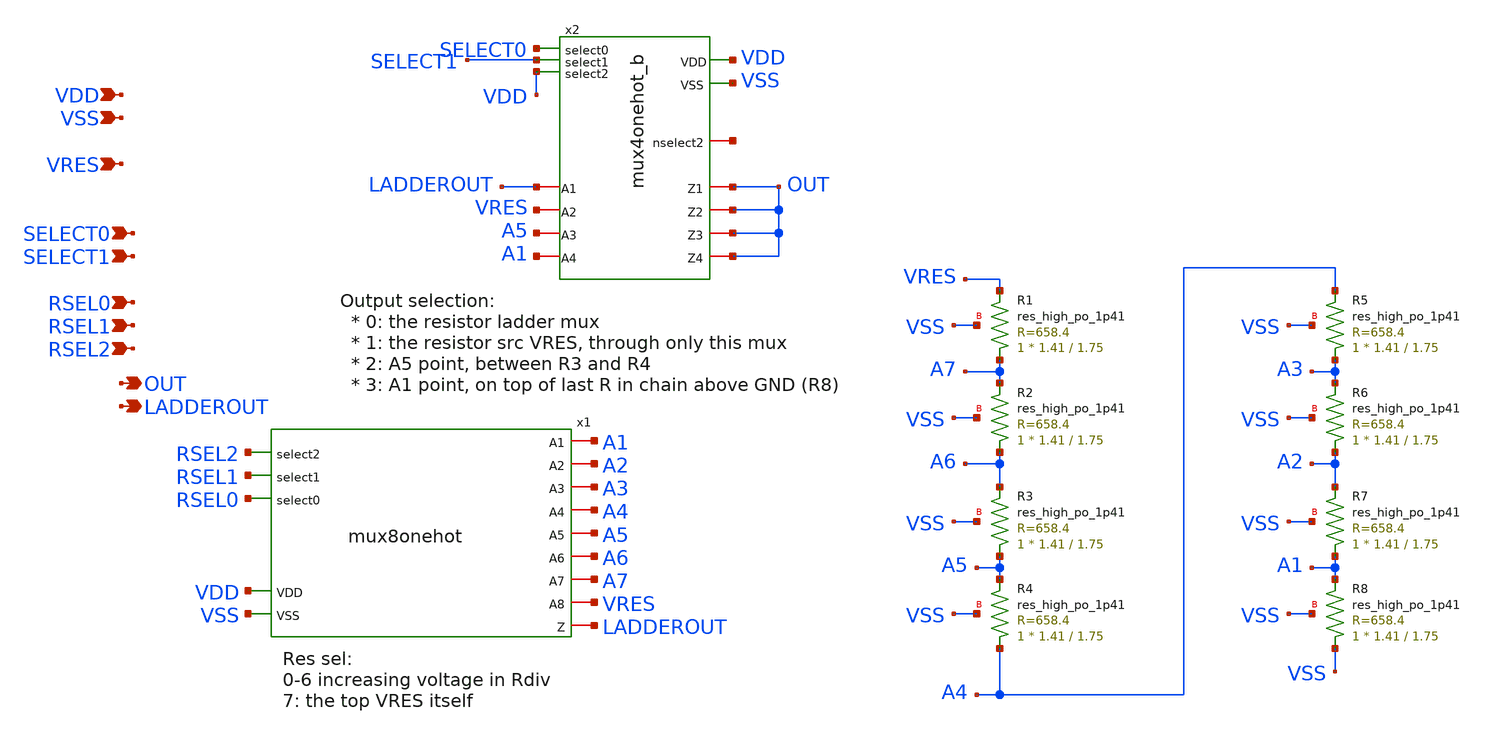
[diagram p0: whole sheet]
** sch_path: xschem/muxtest.sch
**.subckt muxtest VSS VDD SELECT0 SELECT1 VRES RSEL0 RSEL1 RSEL2 OUT LADDEROUT
*.ipin VSS
*.ipin VDD
*.ipin SELECT0
*.ipin SELECT1
*.ipin VRES
*.ipin RSEL0
*.ipin RSEL1
*.ipin RSEL2
*.opin OUT
*.opin LADDEROUT
x1 VDD VSS RSEL0 RSEL1 A1 A5 A6 A2 A7 A3 RSEL2 VRES A4 LADDEROUT mux8onehot
x2 SELECT1 VDD VSS A5 VRES LADDEROUT OUT OUT OUT A1 OUT SELECT0 VDD net1 mux4onehot_b
XR1 A7 VRES VSS sky130_fd_pr__res_high_po_1p41 L=1.75 mult=1 m=1
XR2 A6 A7 VSS sky130_fd_pr__res_high_po_1p41 L=1.75 mult=1 m=1
XR3 A5 A6 VSS sky130_fd_pr__res_high_po_1p41 L=1.75 mult=1 m=1
XR4 A4 A5 VSS sky130_fd_pr__res_high_po_1p41 L=1.75 mult=1 m=1
XR5 A3 A4 VSS sky130_fd_pr__res_high_po_1p41 L=1.75 mult=1 m=1
XR6 A2 A3 VSS sky130_fd_pr__res_high_po_1p41 L=1.75 mult=1 m=1
XR7 A1 A2 VSS sky130_fd_pr__res_high_po_1p41 L=1.75 mult=1 m=1
XR8 VSS A1 VSS sky130_fd_pr__res_high_po_1p41 L=1.75 mult=1 m=1
**.ends
.end
